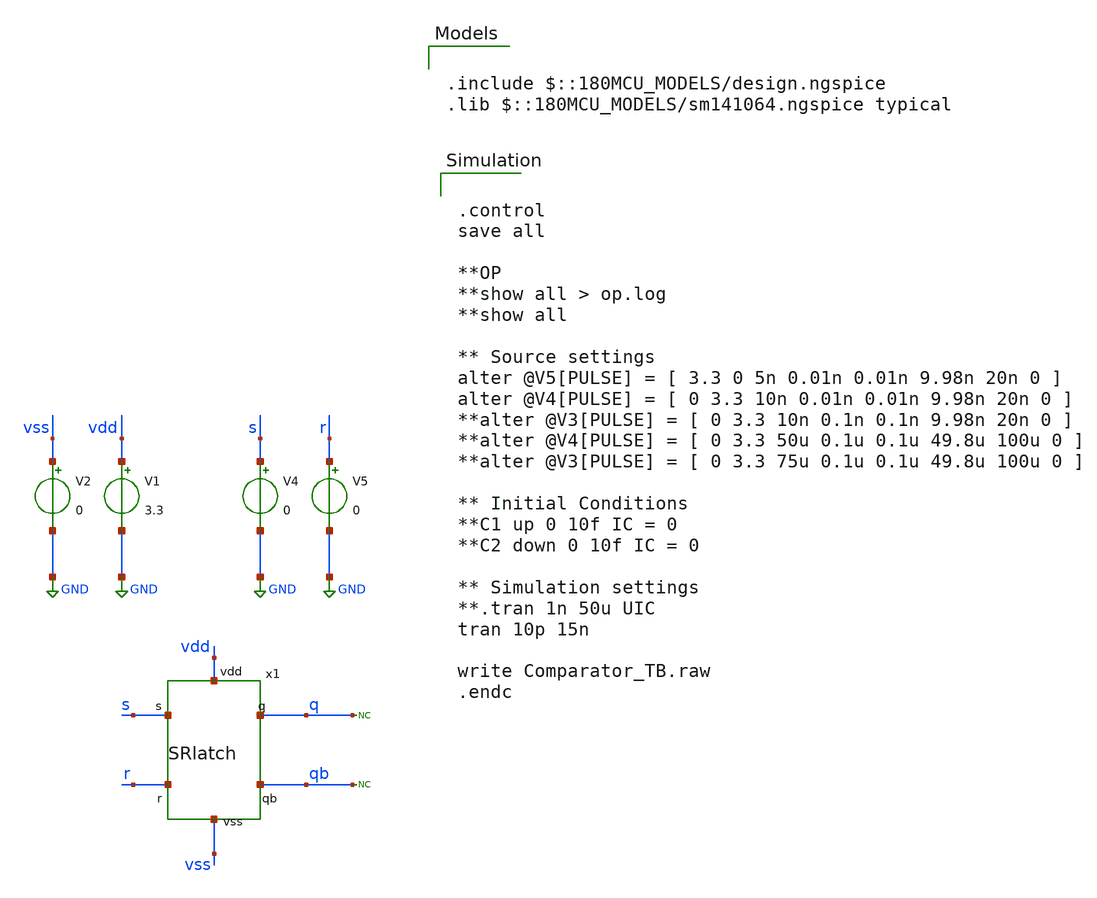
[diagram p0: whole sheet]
** sch_path: designs/libs/qw_core_analog_pkedit/SRlatch_tb.sch
**.subckt SRlatch_tb
x1 vdd s q qb r vss SRlatch
V1 vdd GND 3.3
V2 vss GND 0
V4 s GND 0
V5 r GND 0
* noconn q
* noconn qb
**** begin user architecture code

.include $::180MCU_MODELS/design.ngspice
.lib $::180MCU_MODELS/sm141064.ngspice typical



.control
save all

**OP
**show all > op.log
**show all

** Source settings
alter @V5[PULSE] = [ 3.3 0 5n 0.01n 0.01n 9.98n 20n 0 ]
alter @V4[PULSE] = [ 0 3.3 10n 0.01n 0.01n 9.98n 20n 0 ]
**alter @V3[PULSE] = [ 0 3.3 10n 0.1n 0.1n 9.98n 20n 0 ]
**alter @V4[PULSE] = [ 0 3.3 50u 0.1u 0.1u 49.8u 100u 0 ]
**alter @V3[PULSE] = [ 0 3.3 75u 0.1u 0.1u 49.8u 100u 0 ]

** Initial Conditions
**C1 up 0 10f IC = 0
**C2 down 0 10f IC = 0

** Simulation settings
**.tran 1n 50u UIC
tran 10p 15n

write Comparator_TB.raw
.endc


**** end user architecture code
**.ends

* expanding   symbol:  SRlatch.sym # of pins=6
** sym_path: designs/libs/qw_core_analog_pkedit/SRlatch.sym
** sch_path: designs/libs/qw_core_analog_pkedit/SRlatch.sch
.subckt SRlatch vdd s q qb r vss
*.iopin s
*.iopin r
*.iopin q
*.iopin qb
*.iopin vdd
*.iopin vss
x1 vdd s qb q vss NOR
x2 vdd q r qb vss NOR
.ends


* expanding   symbol:  libs/qw_core_analog/NOR.sym # of pins=5
** sym_path: designs/libs/qw_core_analog_pkedit/NOR.sym
** sch_path: designs/libs/qw_core_analog_pkedit/NOR.sch
.subckt NOR vdd a b out vss
*.iopin vdd
*.iopin vss
*.iopin a
*.iopin b
*.iopin out
XM1 out a vss vss nfet_03v3 L=0.28u W=0.5u nf=1 ad='int((nf+1)/2) * W/nf * 0.18u' as='int((nf+2)/2) * W/nf * 0.18u'
+ pd='2*int((nf+1)/2) * (W/nf + 0.18u)' ps='2*int((nf+2)/2) * (W/nf + 0.18u)' nrd='0.18u / W' nrs='0.18u / W'
+ sa=0 sb=0 sd=0 m=1
XM2 net1 a vdd vdd pfet_03v3 L=0.28u W=2u nf=1 ad='int((nf+1)/2) * W/nf * 0.18u' as='int((nf+2)/2) * W/nf * 0.18u'
+ pd='2*int((nf+1)/2) * (W/nf + 0.18u)' ps='2*int((nf+2)/2) * (W/nf + 0.18u)' nrd='0.18u / W' nrs='0.18u / W'
+ sa=0 sb=0 sd=0 m=1
XM3 out b net1 vdd pfet_03v3 L=0.28u W=2u nf=1 ad='int((nf+1)/2) * W/nf * 0.18u' as='int((nf+2)/2) * W/nf * 0.18u'
+ pd='2*int((nf+1)/2) * (W/nf + 0.18u)' ps='2*int((nf+2)/2) * (W/nf + 0.18u)' nrd='0.18u / W' nrs='0.18u / W'
+ sa=0 sb=0 sd=0 m=1
XM4 out b vss vss nfet_03v3 L=0.28u W=0.5u nf=1 ad='int((nf+1)/2) * W/nf * 0.18u' as='int((nf+2)/2) * W/nf * 0.18u'
+ pd='2*int((nf+1)/2) * (W/nf + 0.18u)' ps='2*int((nf+2)/2) * (W/nf + 0.18u)' nrd='0.18u / W' nrs='0.18u / W'
+ sa=0 sb=0 sd=0 m=1
.ends

.GLOBAL GND
.end
